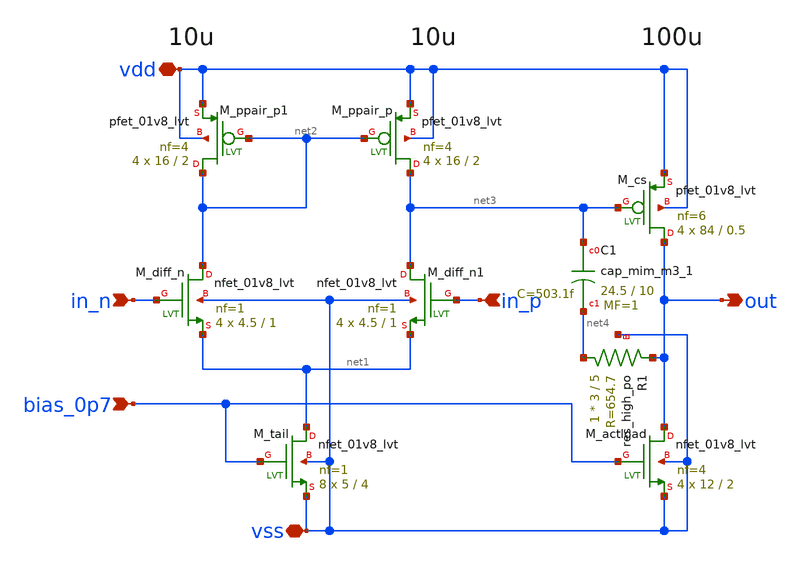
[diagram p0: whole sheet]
** sch_path: design/opamp/opamp_realcomp2_usefinger.sch
**.subckt opamp_realcomp2_usefinger vdd vss in_n in_p out bias_0p7
*.iopin vdd
*.iopin vss
*.ipin in_n
*.ipin in_p
*.opin out
*.ipin bias_0p7
XM_diff_n net2 in_n net1 vss sky130_fd_pr__nfet_01v8_lvt L=1 W=4.5 nf=1 ad='int((nf+1)/2) * W/nf * 0.29'
+ as='int((nf+2)/2) * W/nf * 0.29' pd='2*int((nf+1)/2) * (W/nf + 0.29)' ps='2*int((nf+2)/2) * (W/nf + 0.29)'
+ nrd='0.29 / W' nrs='0.29 / W' sa=0 sb=0 sd=0 mult=4 m=4
XM_diff_n1 net3 in_p net1 vss sky130_fd_pr__nfet_01v8_lvt L=1 W=4.5 nf=1 ad='int((nf+1)/2) * W/nf * 0.29'
+ as='int((nf+2)/2) * W/nf * 0.29' pd='2*int((nf+1)/2) * (W/nf + 0.29)' ps='2*int((nf+2)/2) * (W/nf + 0.29)'
+ nrd='0.29 / W' nrs='0.29 / W' sa=0 sb=0 sd=0 mult=4 m=4
XM_tail net1 bias_0p7 vss vss sky130_fd_pr__nfet_01v8_lvt L=4 W=5 nf=1 ad='int((nf+1)/2) * W/nf * 0.29'
+ as='int((nf+2)/2) * W/nf * 0.29' pd='2*int((nf+1)/2) * (W/nf + 0.29)' ps='2*int((nf+2)/2) * (W/nf + 0.29)'
+ nrd='0.29 / W' nrs='0.29 / W' sa=0 sb=0 sd=0 mult=8 m=8
XM_actload out bias_0p7 vss vss sky130_fd_pr__nfet_01v8_lvt L=2 W=12 nf=4 ad='int((nf+1)/2) * W/nf * 0.29'
+ as='int((nf+2)/2) * W/nf * 0.29' pd='2*int((nf+1)/2) * (W/nf + 0.29)' ps='2*int((nf+2)/2) * (W/nf + 0.29)'
+ nrd='0.29 / W' nrs='0.29 / W' sa=0 sb=0 sd=0 mult=4 m=4
XM_ppair_p net3 net2 vdd vdd sky130_fd_pr__pfet_01v8_lvt L=2 W=16 nf=4 ad='int((nf+1)/2) * W/nf * 0.29'
+ as='int((nf+2)/2) * W/nf * 0.29' pd='2*int((nf+1)/2) * (W/nf + 0.29)' ps='2*int((nf+2)/2) * (W/nf + 0.29)'
+ nrd='0.29 / W' nrs='0.29 / W' sa=0 sb=0 sd=0 mult=4 m=4
XM_ppair_p1 net2 net2 vdd vdd sky130_fd_pr__pfet_01v8_lvt L=2 W=16 nf=4 ad='int((nf+1)/2) * W/nf * 0.29'
+ as='int((nf+2)/2) * W/nf * 0.29' pd='2*int((nf+1)/2) * (W/nf + 0.29)' ps='2*int((nf+2)/2) * (W/nf + 0.29)'
+ nrd='0.29 / W' nrs='0.29 / W' sa=0 sb=0 sd=0 mult=4 m=4
XM_cs out net3 vdd vdd sky130_fd_pr__pfet_01v8_lvt L=0.5 W=84 nf=6 ad='int((nf+1)/2) * W/nf * 0.29' as='int((nf+2)/2) * W/nf * 0.29'
+ pd='2*int((nf+1)/2) * (W/nf + 0.29)' ps='2*int((nf+2)/2) * (W/nf + 0.29)' nrd='0.29 / W' nrs='0.29 / W'
+ sa=0 sb=0 sd=0 mult=4 m=4
XR1 net4 out vss sky130_fd_pr__res_high_po W=3 L=5 mult=1 m=1
XC1 net3 net4 sky130_fd_pr__cap_mim_m3_1 W=24.5 L=10 MF=1 m=1
**.ends
.end
